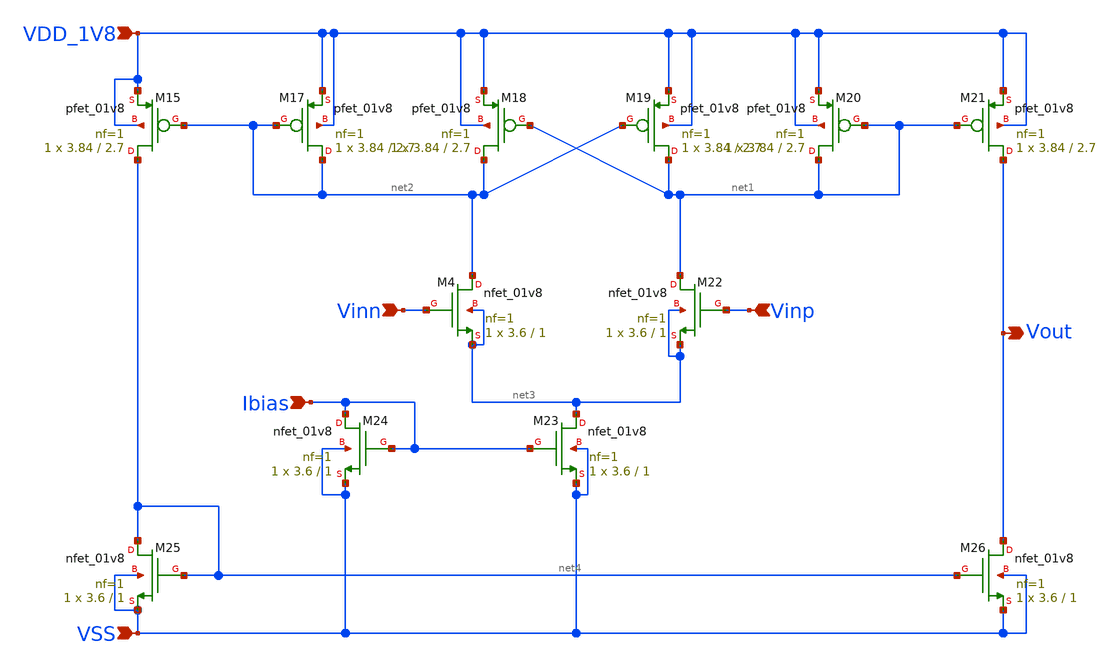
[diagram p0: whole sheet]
** sch_path: design/CNR_GR06_SKY130NM/comparator.sch
**.subckt comparator VDD_1V8 VSS Vinn Ibias Vout Vinp
*.ipin VDD_1V8
*.ipin VSS
*.ipin Vinn
*.ipin Ibias
*.opin Vout
*.ipin Vinp
XM4 net2 Vinn net3 net3 sky130_fd_pr__nfet_01v8 L=1 W=3.6 nf=1 ad='int((nf+1)/2) * W/nf * 0.29' as='int((nf+2)/2) * W/nf * 0.29'
+ pd='2*int((nf+1)/2) * (W/nf + 0.29)' ps='2*int((nf+2)/2) * (W/nf + 0.29)' nrd='0.29 / W' nrs='0.29 / W'
+ sa=0 sb=0 sd=0 mult=1 m=1
XM15 net4 net2 VDD_1V8 VDD_1V8 sky130_fd_pr__pfet_01v8 L=2.7 W=3.84 nf=1 ad='int((nf+1)/2) * W/nf * 0.29'
+ as='int((nf+2)/2) * W/nf * 0.29' pd='2*int((nf+1)/2) * (W/nf + 0.29)' ps='2*int((nf+2)/2) * (W/nf + 0.29)'
+ nrd='0.29 / W' nrs='0.29 / W' sa=0 sb=0 sd=0 mult=1 m=1
XM17 net2 net2 VDD_1V8 VDD_1V8 sky130_fd_pr__pfet_01v8 L=2.7 W=3.84 nf=1 ad='int((nf+1)/2) * W/nf * 0.29'
+ as='int((nf+2)/2) * W/nf * 0.29' pd='2*int((nf+1)/2) * (W/nf + 0.29)' ps='2*int((nf+2)/2) * (W/nf + 0.29)'
+ nrd='0.29 / W' nrs='0.29 / W' sa=0 sb=0 sd=0 mult=1 m=1
XM18 net2 net1 VDD_1V8 VDD_1V8 sky130_fd_pr__pfet_01v8 L=2.7 W=3.84 nf=1 ad='int((nf+1)/2) * W/nf * 0.29'
+ as='int((nf+2)/2) * W/nf * 0.29' pd='2*int((nf+1)/2) * (W/nf + 0.29)' ps='2*int((nf+2)/2) * (W/nf + 0.29)'
+ nrd='0.29 / W' nrs='0.29 / W' sa=0 sb=0 sd=0 mult=1 m=1
XM19 net1 net2 VDD_1V8 VDD_1V8 sky130_fd_pr__pfet_01v8 L=2.7 W=3.84 nf=1 ad='int((nf+1)/2) * W/nf * 0.29'
+ as='int((nf+2)/2) * W/nf * 0.29' pd='2*int((nf+1)/2) * (W/nf + 0.29)' ps='2*int((nf+2)/2) * (W/nf + 0.29)'
+ nrd='0.29 / W' nrs='0.29 / W' sa=0 sb=0 sd=0 mult=1 m=1
XM20 net1 net1 VDD_1V8 VDD_1V8 sky130_fd_pr__pfet_01v8 L=2.7 W=3.84 nf=1 ad='int((nf+1)/2) * W/nf * 0.29'
+ as='int((nf+2)/2) * W/nf * 0.29' pd='2*int((nf+1)/2) * (W/nf + 0.29)' ps='2*int((nf+2)/2) * (W/nf + 0.29)'
+ nrd='0.29 / W' nrs='0.29 / W' sa=0 sb=0 sd=0 mult=1 m=1
XM21 Vout net1 VDD_1V8 VDD_1V8 sky130_fd_pr__pfet_01v8 L=2.7 W=3.84 nf=1 ad='int((nf+1)/2) * W/nf * 0.29'
+ as='int((nf+2)/2) * W/nf * 0.29' pd='2*int((nf+1)/2) * (W/nf + 0.29)' ps='2*int((nf+2)/2) * (W/nf + 0.29)'
+ nrd='0.29 / W' nrs='0.29 / W' sa=0 sb=0 sd=0 mult=1 m=1
XM22 net1 Vinp net3 net3 sky130_fd_pr__nfet_01v8 L=1 W=3.6 nf=1 ad='int((nf+1)/2) * W/nf * 0.29' as='int((nf+2)/2) * W/nf * 0.29'
+ pd='2*int((nf+1)/2) * (W/nf + 0.29)' ps='2*int((nf+2)/2) * (W/nf + 0.29)' nrd='0.29 / W' nrs='0.29 / W'
+ sa=0 sb=0 sd=0 mult=1 m=1
XM23 net3 Ibias VSS VSS sky130_fd_pr__nfet_01v8 L=1 W=3.6 nf=1 ad='int((nf+1)/2) * W/nf * 0.29' as='int((nf+2)/2) * W/nf * 0.29'
+ pd='2*int((nf+1)/2) * (W/nf + 0.29)' ps='2*int((nf+2)/2) * (W/nf + 0.29)' nrd='0.29 / W' nrs='0.29 / W'
+ sa=0 sb=0 sd=0 mult=1 m=1
XM24 Ibias Ibias VSS VSS sky130_fd_pr__nfet_01v8 L=1 W=3.6 nf=1 ad='int((nf+1)/2) * W/nf * 0.29' as='int((nf+2)/2) * W/nf * 0.29'
+ pd='2*int((nf+1)/2) * (W/nf + 0.29)' ps='2*int((nf+2)/2) * (W/nf + 0.29)' nrd='0.29 / W' nrs='0.29 / W'
+ sa=0 sb=0 sd=0 mult=1 m=1
XM25 net4 net4 VSS VSS sky130_fd_pr__nfet_01v8 L=1 W=3.6 nf=1 ad='int((nf+1)/2) * W/nf * 0.29' as='int((nf+2)/2) * W/nf * 0.29'
+ pd='2*int((nf+1)/2) * (W/nf + 0.29)' ps='2*int((nf+2)/2) * (W/nf + 0.29)' nrd='0.29 / W' nrs='0.29 / W'
+ sa=0 sb=0 sd=0 mult=1 m=1
XM26 Vout net4 VSS VSS sky130_fd_pr__nfet_01v8 L=1 W=3.6 nf=1 ad='int((nf+1)/2) * W/nf * 0.29' as='int((nf+2)/2) * W/nf * 0.29'
+ pd='2*int((nf+1)/2) * (W/nf + 0.29)' ps='2*int((nf+2)/2) * (W/nf + 0.29)' nrd='0.29 / W' nrs='0.29 / W'
+ sa=0 sb=0 sd=0 mult=1 m=1
**.ends
.end
